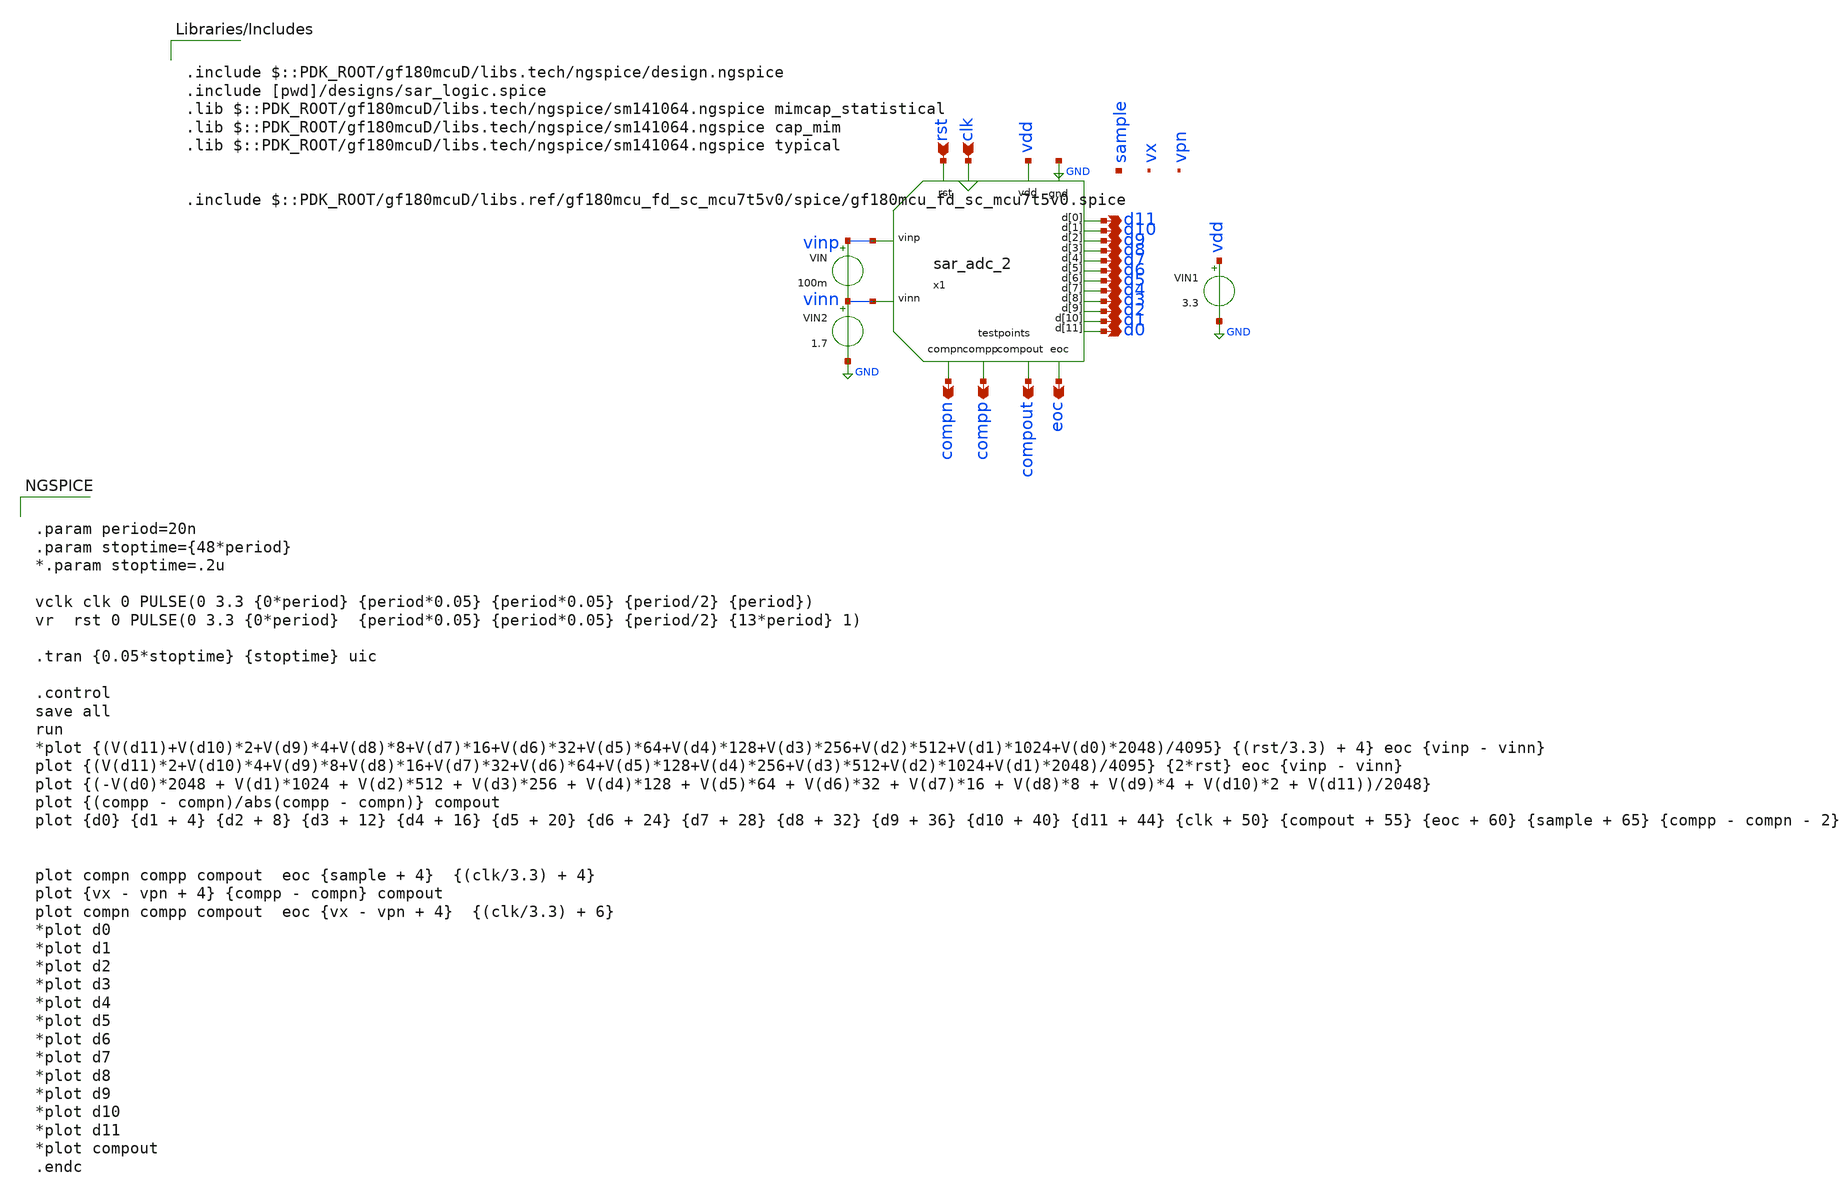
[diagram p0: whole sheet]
** sch_path: xschem/test/tb_sar_adc.sch
**.subckt tb_sar_adc rst clk d0 d1 d2 d3 d4 d5 d6 d7 d8 d9 d10 d11 compn compp compout eoc
*.ipin rst
*.ipin clk
*.opin d0
*.opin d1
*.opin d2
*.opin d3
*.opin d4
*.opin d5
*.opin d6
*.opin d7
*.opin d8
*.opin d9
*.opin d10
*.opin d11
*.opin compn
*.opin compp
*.opin compout
*.opin eoc
x1 vinp d11 rst clk vinn GND vdd d10 d9 d8 d7 d6 d5 d4 d3 d2 d1 d0 compn compp compout eoc sample
+ sar_adc_2
VIN vinp vinn 100m
VIN1 vdd GND 3.3
VIN2 vinn GND 1.7
**** begin user architecture code


.param period=20n
.param stoptime={48*period}
*.param stoptime=.2u

vclk clk 0 PULSE(0 3.3 {0*period} {period*0.05} {period*0.05} {period/2} {period})
vr  rst 0 PULSE(0 3.3 {0*period}  {period*0.05} {period*0.05} {period/2} {13*period} 1)

.tran {0.05*stoptime} {stoptime} uic

.control
save all
run
*plot {(V(d11)+V(d10)*2+V(d9)*4+V(d8)*8+V(d7)*16+V(d6)*32+V(d5)*64+V(d4)*128+V(d3)*256+V(d2)*512+V(d1)*1024+V(d0)*2048)/4095}
*+ {(rst/3.3) + 4} eoc {vinp - vinn}
plot {(V(d11)*2+V(d10)*4+V(d9)*8+V(d8)*16+V(d7)*32+V(d6)*64+V(d5)*128+V(d4)*256+V(d3)*512+V(d2)*1024+V(d1)*2048)/4095}
+ {2*rst} eoc {vinp - vinn}
plot {(-V(d0)*2048 + V(d1)*1024 + V(d2)*512 + V(d3)*256 + V(d4)*128 + V(d5)*64 + V(d6)*32 + V(d7)*16 + V(d8)*8 + V(d9)*4 + V(d10)*2 + V(d11))/2048}
plot {(compp - compn)/abs(compp - compn)} compout
plot {d0} {d1 + 4} {d2 + 8} {d3 + 12} {d4 + 16} {d5 + 20} {d6 + 24} {d7 + 28} {d8 + 32} {d9 + 36} {d10 + 40}
+ {d11 + 44} {clk + 50} {compout + 55} {eoc + 60} {sample + 65} {compp - compn - 2}


plot compn compp compout  eoc {sample + 4}  {(clk/3.3) + 4}
plot {vx - vpn + 4} {compp - compn} compout
plot compn compp compout  eoc {vx - vpn + 4}  {(clk/3.3) + 6}
*plot d0
*plot d1
*plot d2
*plot d3
*plot d4
*plot d5
*plot d6
*plot d7
*plot d8
*plot d9
*plot d10
*plot d11
*plot compout
.endc



.include $::PDK_ROOT/gf180mcuD/libs.tech/ngspice/design.ngspice
.include [pwd]/designs/sar_logic.spice
.lib $::PDK_ROOT/gf180mcuD/libs.tech/ngspice/sm141064.ngspice mimcap_statistical
.lib $::PDK_ROOT/gf180mcuD/libs.tech/ngspice/sm141064.ngspice cap_mim
.lib $::PDK_ROOT/gf180mcuD/libs.tech/ngspice/sm141064.ngspice typical


.include $::PDK_ROOT/gf180mcuD/libs.ref/gf180mcu_fd_sc_mcu7t5v0/spice/gf180mcu_fd_sc_mcu7t5v0.spice


**** end user architecture code
**.ends
.GLOBAL GND
.end
